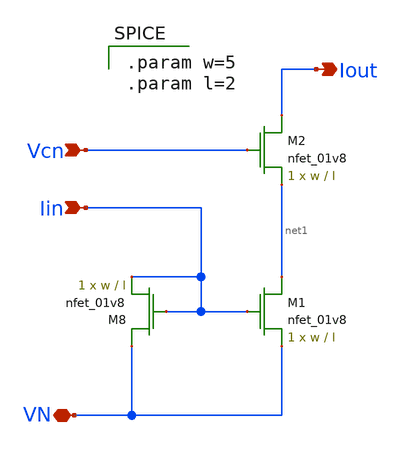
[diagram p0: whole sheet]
** sch_path: schematic/old/iout_mirror2.sch
**.subckt iout_mirror2 VN Iout Iin Vcn
*.iopin VN
*.opin Iout
*.ipin Iin
*.ipin Vcn
XM8 VN Iin Iin GND sky130_fd_pr__nfet_01v8 L=l W=w nf=1 ad='int((nf+1)/2) * W/nf * 0.29' as='int((nf+2)/2) * W/nf * 0.29'
+ pd='2*int((nf+1)/2) * (W/nf + 0.29)' ps='2*int((nf+2)/2) * (W/nf + 0.29)' nrd='0.29 / W' nrs='0.29 / W'
+ sa=0 sb=0 sd=0 mult=1 m=1
XM1 net1 Iin VN GND sky130_fd_pr__nfet_01v8 L=l W=w nf=1 ad='int((nf+1)/2) * W/nf * 0.29' as='int((nf+2)/2) * W/nf * 0.29'
+ pd='2*int((nf+1)/2) * (W/nf + 0.29)' ps='2*int((nf+2)/2) * (W/nf + 0.29)' nrd='0.29 / W' nrs='0.29 / W'
+ sa=0 sb=0 sd=0 mult=1 m=1
XM2 Iout Vcn net1 GND sky130_fd_pr__nfet_01v8 L=l W=w nf=1 ad='int((nf+1)/2) * W/nf * 0.29' as='int((nf+2)/2) * W/nf * 0.29'
+ pd='2*int((nf+1)/2) * (W/nf + 0.29)' ps='2*int((nf+2)/2) * (W/nf + 0.29)' nrd='0.29 / W' nrs='0.29 / W'
+ sa=0 sb=0 sd=0 mult=1 m=1
**** begin user architecture code

.param w=5
.param l=2

**** end user architecture code
**.ends
.end
